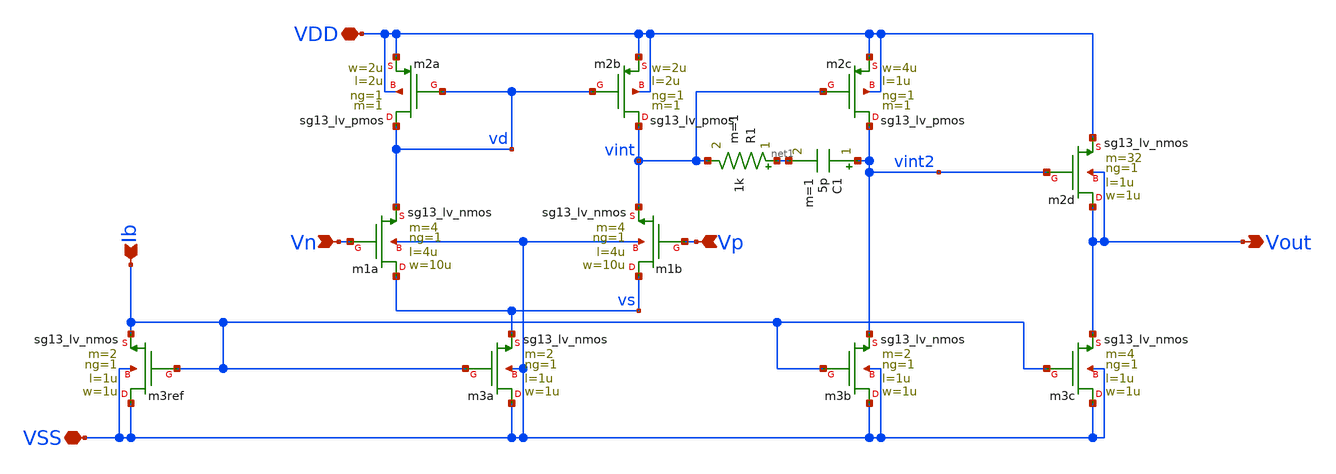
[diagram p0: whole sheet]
** sch_path: ota-5t.sch
**.subckt ota-5t VDD Vn Vout Vp VSS Ib
*.iopin VDD
*.ipin Vn
*.opin Vout
*.ipin Vp
*.iopin VSS
*.ipin Ib
Xm1a vs Vn vd VSS sg13_lv_nmos w=10u l=4u ng=1 m=4 mm_ok=1
Xm2b vint vd VDD VDD sg13_lv_pmos w=2u l=2u ng=1 m=1 mm_ok=1
Xm2a vd vd VDD VDD sg13_lv_pmos w=2u l=2u ng=1 m=1 mm_ok=1
Xm3a VSS Ib vs VSS sg13_lv_nmos w=1u l=1u ng=1 m=2 mm_ok=1
Xm1b vs Vp vint VSS sg13_lv_nmos w=10u l=4u ng=1 m=4 mm_ok=1
Xm3ref VSS Ib Ib VSS sg13_lv_nmos w=1u l=1u ng=1 m=2 mm_ok=1
Xm3b VSS Ib vint2 VSS sg13_lv_nmos w=1u l=1u ng=1 m=2 mm_ok=1
Xm2c vint2 vint VDD VDD sg13_lv_pmos w=4u l=1u ng=1 m=1 mm_ok=1
Xm2d Vout vint2 VDD Vout sg13_lv_nmos w=1u l=1u ng=1 m=32 mm_ok=1
Xm3c VSS Ib Vout VSS sg13_lv_nmos w=1u l=1u ng=1 m=4 mm_ok=1
C1 vint2 net1 5p m=1
R1 net1 vint 1k m=1
**.ends
.end
